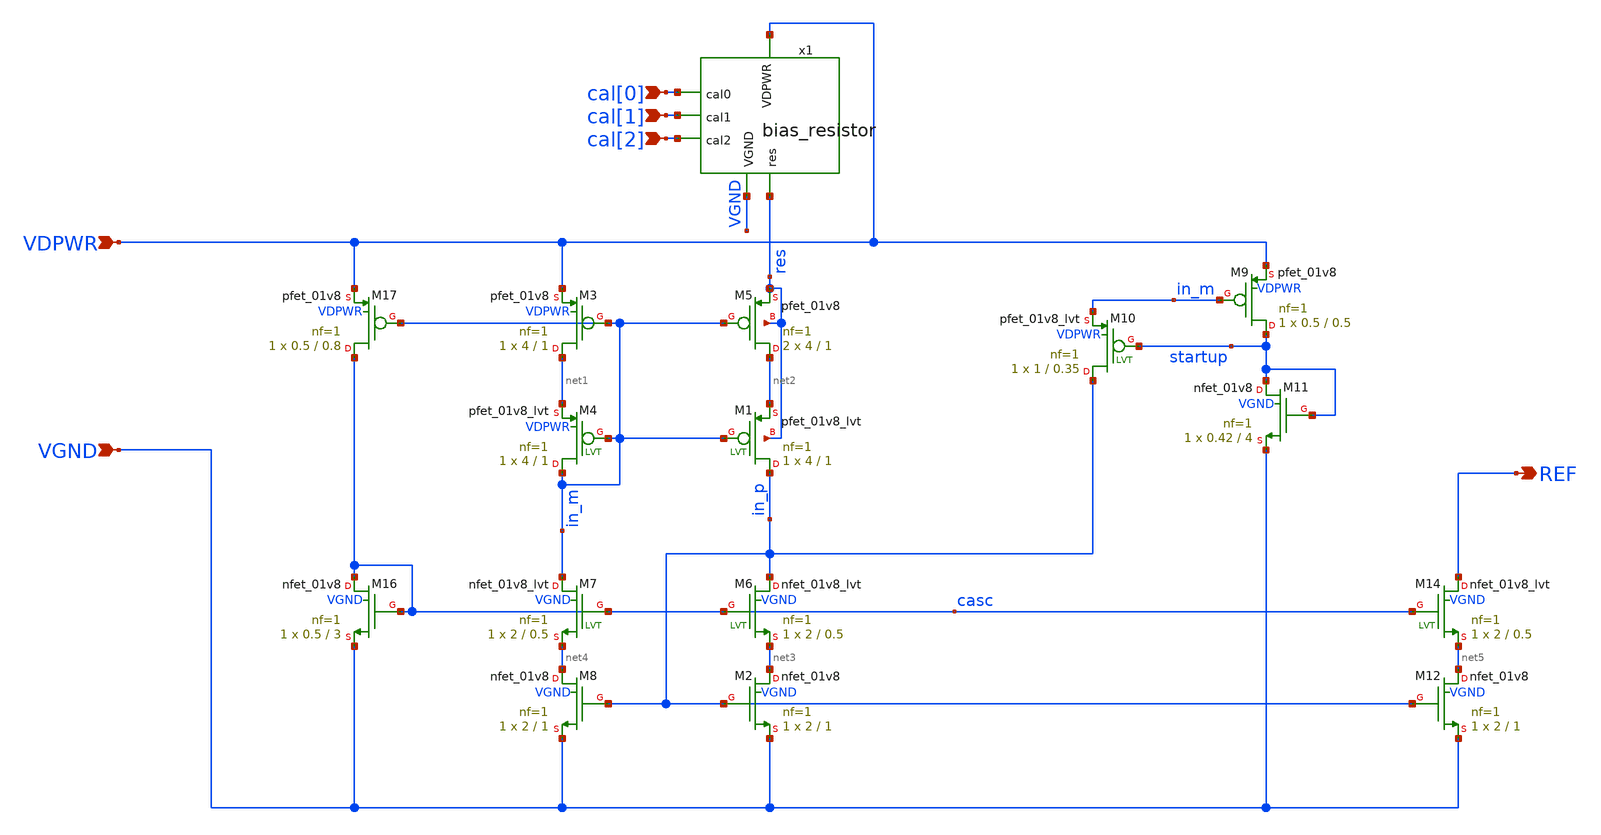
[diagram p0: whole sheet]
** sch_path: xschem/bias.sch
**.subckt bias VDPWR VGND REF cal[0] cal[1] cal[2]
*.ipin VDPWR
*.ipin VGND
*.opin REF
*.ipin cal[0]
*.ipin cal[1]
*.ipin cal[2]
XM4 in_m in_m net1 VDPWR sky130_fd_pr__pfet_01v8_lvt L=1 W=4 nf=1 ad='int((1 + 1)/2) * 4 / 1 * 0.29'
+ as='int((1 + 2)/2) * 4 / 1 * 0.29' pd='2*int((1 + 1)/2) * (4 / 1 + 0.29)' ps='2*int((1 + 2)/2) * (4 / 1 + 0.29)'
+ nrd='0.29 / 4 ' nrs='0.29 / 4 ' sa=0 sb=0 sd=0 mult=1 m=1
XM1 in_p in_m net2 res sky130_fd_pr__pfet_01v8_lvt L=1 W=4 nf=1 ad='int((1 + 1)/2) * 4 / 1 * 0.29' as='int((1 + 2)/2) * 4 / 1 * 0.29'
+ pd='2*int((1 + 1)/2) * (4 / 1 + 0.29)' ps='2*int((1 + 2)/2) * (4 / 1 + 0.29)' nrd='0.29 / 4 ' nrs='0.29 / 4 '
+ sa=0 sb=0 sd=0 mult=1 m=1
XM8 net4 in_p VGND VGND sky130_fd_pr__nfet_01v8 L=1 W=2 nf=1 ad='int((1 + 1)/2) * 2 / 1 * 0.29' as='int((1 + 2)/2) * 2 / 1 * 0.29'
+ pd='2*int((1 + 1)/2) * (2 / 1 + 0.29)' ps='2*int((1 + 2)/2) * (2 / 1 + 0.29)' nrd='0.29 / 2 ' nrs='0.29 / 2 '
+ sa=0 sb=0 sd=0 mult=1 m=1
XM2 net3 in_p VGND VGND sky130_fd_pr__nfet_01v8 L=1 W=2 nf=1 ad='int((1 + 1)/2) * 2 / 1 * 0.29' as='int((1 + 2)/2) * 2 / 1 * 0.29'
+ pd='2*int((1 + 1)/2) * (2 / 1 + 0.29)' ps='2*int((1 + 2)/2) * (2 / 1 + 0.29)' nrd='0.29 / 2 ' nrs='0.29 / 2 '
+ sa=0 sb=0 sd=0 mult=1 m=1
XM11 startup startup VGND VGND sky130_fd_pr__nfet_01v8 L=4 W=0.42 nf=1 ad='int((1 + 1)/2) * 0.42 / 1 * 0.29'
+ as='int((1 + 2)/2) * 0.42 / 1 * 0.29' pd='2*int((1 + 1)/2) * (0.42 / 1 + 0.29)' ps='2*int((1 + 2)/2) * (0.42 / 1 + 0.29)'
+ nrd='0.29 / 0.42 ' nrs='0.29 / 0.42 ' sa=0 sb=0 sd=0 mult=1 m=1
XM12 net5 in_p VGND VGND sky130_fd_pr__nfet_01v8 L=1 W=2 nf=1 ad='int((1 + 1)/2) * 2 / 1 * 0.29' as='int((1 + 2)/2) * 2 / 1 * 0.29'
+ pd='2*int((1 + 1)/2) * (2 / 1 + 0.29)' ps='2*int((1 + 2)/2) * (2 / 1 + 0.29)' nrd='0.29 / 2 ' nrs='0.29 / 2 '
+ sa=0 sb=0 sd=0 mult=1 m=1
XM9 startup in_m VDPWR VDPWR sky130_fd_pr__pfet_01v8 L=0.5 W=0.5 nf=1 ad='int((1 + 1)/2) * 0.5 / 1 * 0.29'
+ as='int((1 + 2)/2) * 0.5 / 1 * 0.29' pd='2*int((1 + 1)/2) * (0.5 / 1 + 0.29)' ps='2*int((1 + 2)/2) * (0.5 / 1 + 0.29)'
+ nrd='0.29 / 0.5 ' nrs='0.29 / 0.5 ' sa=0 sb=0 sd=0 mult=1 m=1
XM10 in_p startup in_m VDPWR sky130_fd_pr__pfet_01v8_lvt L=0.35 W=1 nf=1 ad='int((1 + 1)/2) * 1 / 1 * 0.29'
+ as='int((1 + 2)/2) * 1 / 1 * 0.29' pd='2*int((1 + 1)/2) * (1 / 1 + 0.29)' ps='2*int((1 + 2)/2) * (1 / 1 + 0.29)'
+ nrd='0.29 / 1 ' nrs='0.29 / 1 ' sa=0 sb=0 sd=0 mult=1 m=1
XM3 net1 in_m VDPWR VDPWR sky130_fd_pr__pfet_01v8 L=1 W=4 nf=1 ad='int((1 + 1)/2) * 4 / 1 * 0.29' as='int((1 + 2)/2) * 4 / 1 * 0.29'
+ pd='2*int((1 + 1)/2) * (4 / 1 + 0.29)' ps='2*int((1 + 2)/2) * (4 / 1 + 0.29)' nrd='0.29 / 4 ' nrs='0.29 / 4 '
+ sa=0 sb=0 sd=0 mult=1 m=1
XM5 net2 in_m res res sky130_fd_pr__pfet_01v8 L=1 W=4 nf=1 ad='int((1 + 1)/2) * 4 / 1 * 0.29' as='int((1 + 2)/2) * 4 / 1 * 0.29'
+ pd='2*int((1 + 1)/2) * (4 / 1 + 0.29)' ps='2*int((1 + 2)/2) * (4 / 1 + 0.29)' nrd='0.29 / 4 ' nrs='0.29 / 4 '
+ sa=0 sb=0 sd=0 mult=2 m=2
XM6 in_p casc net3 VGND sky130_fd_pr__nfet_01v8_lvt L=0.5 W=2 nf=1 ad='int((1 + 1)/2) * 2 / 1 * 0.29'
+ as='int((1 + 2)/2) * 2 / 1 * 0.29' pd='2*int((1 + 1)/2) * (2 / 1 + 0.29)' ps='2*int((1 + 2)/2) * (2 / 1 + 0.29)'
+ nrd='0.29 / 2 ' nrs='0.29 / 2 ' sa=0 sb=0 sd=0 mult=1 m=1
XM7 in_m casc net4 VGND sky130_fd_pr__nfet_01v8_lvt L=0.5 W=2 nf=1 ad='int((1 + 1)/2) * 2 / 1 * 0.29'
+ as='int((1 + 2)/2) * 2 / 1 * 0.29' pd='2*int((1 + 1)/2) * (2 / 1 + 0.29)' ps='2*int((1 + 2)/2) * (2 / 1 + 0.29)'
+ nrd='0.29 / 2 ' nrs='0.29 / 2 ' sa=0 sb=0 sd=0 mult=1 m=1
XM14 REF casc net5 VGND sky130_fd_pr__nfet_01v8_lvt L=0.5 W=2 nf=1 ad='int((1 + 1)/2) * 2 / 1 * 0.29'
+ as='int((1 + 2)/2) * 2 / 1 * 0.29' pd='2*int((1 + 1)/2) * (2 / 1 + 0.29)' ps='2*int((1 + 2)/2) * (2 / 1 + 0.29)'
+ nrd='0.29 / 2 ' nrs='0.29 / 2 ' sa=0 sb=0 sd=0 mult=1 m=1
XM16 casc casc VGND VGND sky130_fd_pr__nfet_01v8 L=3 W=0.5 nf=1 ad='int((1 + 1)/2) * 0.5 / 1 * 0.29'
+ as='int((1 + 2)/2) * 0.5 / 1 * 0.29' pd='2*int((1 + 1)/2) * (0.5 / 1 + 0.29)' ps='2*int((1 + 2)/2) * (0.5 / 1 + 0.29)'
+ nrd='0.29 / 0.5 ' nrs='0.29 / 0.5 ' sa=0 sb=0 sd=0 mult=1 m=1
XM17 casc in_m VDPWR VDPWR sky130_fd_pr__pfet_01v8 L=0.8 W=0.5 nf=1 ad='int((1 + 1)/2) * 0.5 / 1 * 0.29'
+ as='int((1 + 2)/2) * 0.5 / 1 * 0.29' pd='2*int((1 + 1)/2) * (0.5 / 1 + 0.29)' ps='2*int((1 + 2)/2) * (0.5 / 1 + 0.29)'
+ nrd='0.29 / 0.5 ' nrs='0.29 / 0.5 ' sa=0 sb=0 sd=0 mult=1 m=1
x1 VDPWR cal[0] cal[1] cal[2] res VGND bias_resistor
**.ends

* expanding   symbol:  /foss/designs/ttsky26c-analog-park/xschem/bias_resistor.sym # of pins=6
** sym_path: xschem/bias_resistor.sym
** sch_path: xschem/bias_resistor.sch
.subckt bias_resistor VDPWR cal0 cal1 cal2 res VGND
*.ipin VDPWR
*.ipin cal0
*.ipin cal1
*.ipin cal2
*.ipin res
*.ipin VGND
XR2 net1 net7 VDPWR sky130_fd_pr__res_high_po_0p69 L=2.5 mult=1 m=1
XR1 net7 VDPWR VDPWR sky130_fd_pr__res_xhigh_po_5p73 L=0.505 mult=1 m=1
XR3 net8 net1 VDPWR sky130_fd_pr__res_xhigh_po_2p85 L=1 mult=1 m=1
XR4 net2 net8 VDPWR sky130_fd_pr__res_high_po_0p69 L=4.6 mult=1 m=1
XM1 net1 net4 VDPWR VDPWR sky130_fd_pr__pfet_01v8 L=0.15 W=4 nf=2 ad='int((2 + 1)/2) * 4 / 2 * 0.29'
+ as='int((2 + 2)/2) * 4 / 2 * 0.29' pd='2*int((2 + 1)/2) * (4 / 2 + 0.29)' ps='2*int((2 + 2)/2) * (4 / 2 + 0.29)'
+ nrd='0.29 / 4 ' nrs='0.29 / 4 ' sa=0 sb=0 sd=0 mult=1 m=1
XR5 net9 net2 VDPWR sky130_fd_pr__res_xhigh_po_2p85 L=1.8 mult=1 m=1
XR6 net10 net9 VDPWR sky130_fd_pr__res_high_po_0p69 L=4.3 mult=1 m=1
XR7 net3 net10 VDPWR sky130_fd_pr__res_high_po_0p69 L=4.3 mult=1 m=1
XR8 net11 net3 VDPWR sky130_fd_pr__res_xhigh_po_2p85 L=1.8 mult=1 m=1
XR9 net12 net11 VDPWR sky130_fd_pr__res_high_po_0p69 L=3.8 mult=1 m=1
XR10 res net12 VDPWR sky130_fd_pr__res_high_po_0p69 L=3.8 mult=1 m=1
XM2 net2 net5 net1 VDPWR sky130_fd_pr__pfet_01v8 L=0.15 W=4 nf=2 ad='int((2 + 1)/2) * 4 / 2 * 0.29' as='int((2 + 2)/2) * 4 / 2 * 0.29'
+ pd='2*int((2 + 1)/2) * (4 / 2 + 0.29)' ps='2*int((2 + 2)/2) * (4 / 2 + 0.29)' nrd='0.29 / 4 ' nrs='0.29 / 4 '
+ sa=0 sb=0 sd=0 mult=1 m=1
XM3 net3 net6 net2 VDPWR sky130_fd_pr__pfet_01v8 L=0.15 W=4 nf=2 ad='int((2 + 1)/2) * 4 / 2 * 0.29' as='int((2 + 2)/2) * 4 / 2 * 0.29'
+ pd='2*int((2 + 1)/2) * (4 / 2 + 0.29)' ps='2*int((2 + 2)/2) * (4 / 2 + 0.29)' nrd='0.29 / 4 ' nrs='0.29 / 4 '
+ sa=0 sb=0 sd=0 mult=1 m=1
x1 cal0 VGND VGND VDPWR VDPWR net4 sky130_fd_sc_hd__inv_1
x2 cal1 VGND VGND VDPWR VDPWR net5 sky130_fd_sc_hd__inv_1
x3 cal2 VGND VGND VDPWR VDPWR net6 sky130_fd_sc_hd__inv_1
.ends

.end
